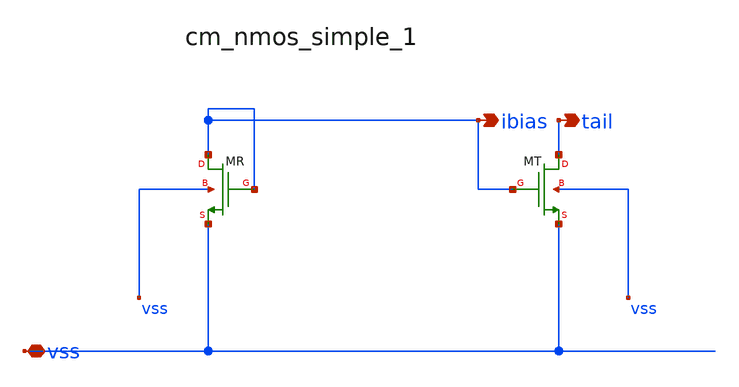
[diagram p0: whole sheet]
** sch_path: analog-db/raw/dp_001_resistive_load/hier/blocks/cm_nmos_simple_1.sch
**.subckt cm_nmos_simple_1 vss ibias tail
*.iopin vss
*.opin ibias
*.opin tail
XMR ibias ibias vss vss sg13_lv_nmos w=x_dut_xmr_w l=x_dut_xmr_l ng=1 m=x_dut_xmr_m
XMT tail ibias vss vss sg13_lv_nmos w=x_dut_xmt_w l=x_dut_xmt_l ng=1 m=x_dut_xmt_m
**.ends
.end
